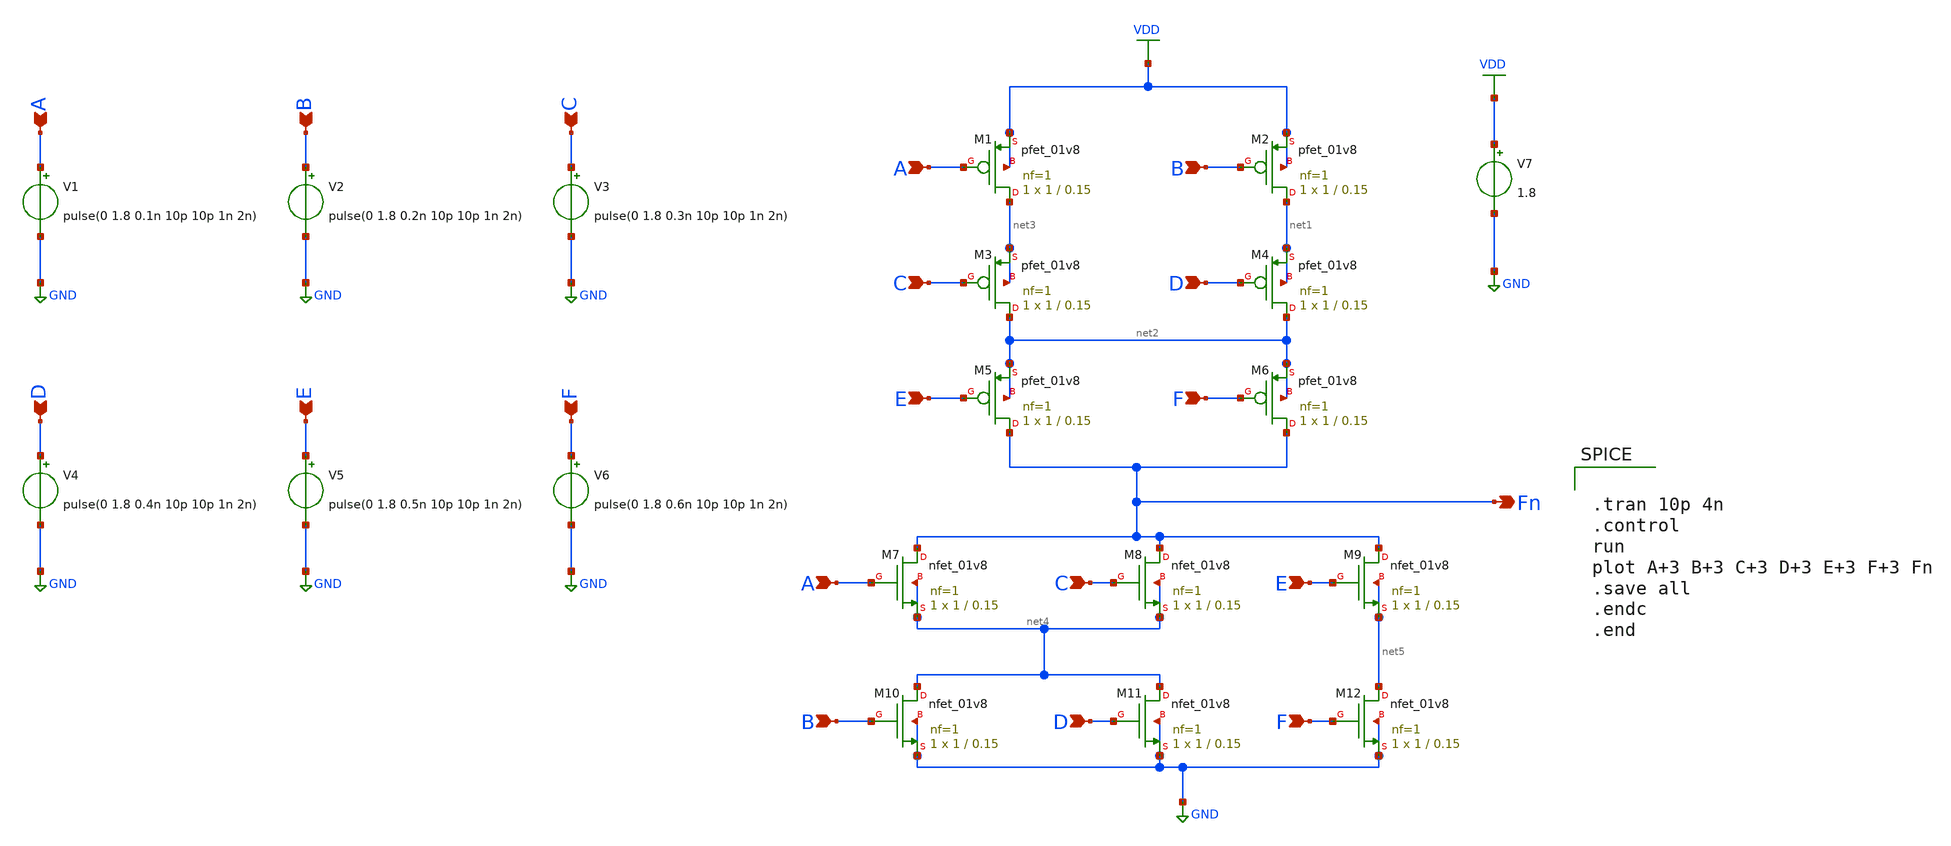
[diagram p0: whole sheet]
** sch_path: Week_1/Function_PreLayout/function_pre.sch
**.subckt function_pre A B A B C D E F A B C D E F Fn C D E F
*.ipin A
*.ipin B
*.ipin A
*.ipin B
*.ipin C
*.ipin D
*.ipin E
*.ipin F
*.ipin A
*.ipin B
*.ipin C
*.ipin D
*.ipin E
*.ipin F
*.opin Fn
*.ipin C
*.ipin D
*.ipin E
*.ipin F
V1 A GND pulse(0 1.8 0.1n 10p 10p 1n 2n)
V2 B GND pulse(0 1.8 0.2n 10p 10p 1n 2n)
XM1 net3 A VDD VDD sky130_fd_pr__pfet_01v8 L=0.15 W=1 nf=1 ad='int((nf+1)/2) * W/nf * 0.29' as='int((nf+2)/2) * W/nf * 0.29'
+ pd='2*int((nf+1)/2) * (W/nf + 0.29)' ps='2*int((nf+2)/2) * (W/nf + 0.29)' nrd='0.29 / W' nrs='0.29 / W'
+ sa=0 sb=0 sd=0 mult=1 m=1
XM2 net1 B VDD VDD sky130_fd_pr__pfet_01v8 L=0.15 W=1 nf=1 ad='int((nf+1)/2) * W/nf * 0.29' as='int((nf+2)/2) * W/nf * 0.29'
+ pd='2*int((nf+1)/2) * (W/nf + 0.29)' ps='2*int((nf+2)/2) * (W/nf + 0.29)' nrd='0.29 / W' nrs='0.29 / W'
+ sa=0 sb=0 sd=0 mult=1 m=1
XM3 net2 C net3 net3 sky130_fd_pr__pfet_01v8 L=0.15 W=1 nf=1 ad='int((nf+1)/2) * W/nf * 0.29' as='int((nf+2)/2) * W/nf * 0.29'
+ pd='2*int((nf+1)/2) * (W/nf + 0.29)' ps='2*int((nf+2)/2) * (W/nf + 0.29)' nrd='0.29 / W' nrs='0.29 / W'
+ sa=0 sb=0 sd=0 mult=1 m=1
XM4 net2 D net1 net1 sky130_fd_pr__pfet_01v8 L=0.15 W=1 nf=1 ad='int((nf+1)/2) * W/nf * 0.29' as='int((nf+2)/2) * W/nf * 0.29'
+ pd='2*int((nf+1)/2) * (W/nf + 0.29)' ps='2*int((nf+2)/2) * (W/nf + 0.29)' nrd='0.29 / W' nrs='0.29 / W'
+ sa=0 sb=0 sd=0 mult=1 m=1
XM5 Fn E net2 net2 sky130_fd_pr__pfet_01v8 L=0.15 W=1 nf=1 ad='int((nf+1)/2) * W/nf * 0.29' as='int((nf+2)/2) * W/nf * 0.29'
+ pd='2*int((nf+1)/2) * (W/nf + 0.29)' ps='2*int((nf+2)/2) * (W/nf + 0.29)' nrd='0.29 / W' nrs='0.29 / W'
+ sa=0 sb=0 sd=0 mult=1 m=1
XM6 Fn F net2 net2 sky130_fd_pr__pfet_01v8 L=0.15 W=1 nf=1 ad='int((nf+1)/2) * W/nf * 0.29' as='int((nf+2)/2) * W/nf * 0.29'
+ pd='2*int((nf+1)/2) * (W/nf + 0.29)' ps='2*int((nf+2)/2) * (W/nf + 0.29)' nrd='0.29 / W' nrs='0.29 / W'
+ sa=0 sb=0 sd=0 mult=1 m=1
XM7 Fn A net4 net4 sky130_fd_pr__nfet_01v8 L=0.15 W=1 nf=1 ad='int((nf+1)/2) * W/nf * 0.29' as='int((nf+2)/2) * W/nf * 0.29'
+ pd='2*int((nf+1)/2) * (W/nf + 0.29)' ps='2*int((nf+2)/2) * (W/nf + 0.29)' nrd='0.29 / W' nrs='0.29 / W'
+ sa=0 sb=0 sd=0 mult=1 m=1
XM8 Fn C net4 net4 sky130_fd_pr__nfet_01v8 L=0.15 W=1 nf=1 ad='int((nf+1)/2) * W/nf * 0.29' as='int((nf+2)/2) * W/nf * 0.29'
+ pd='2*int((nf+1)/2) * (W/nf + 0.29)' ps='2*int((nf+2)/2) * (W/nf + 0.29)' nrd='0.29 / W' nrs='0.29 / W'
+ sa=0 sb=0 sd=0 mult=1 m=1
XM9 Fn E net5 net5 sky130_fd_pr__nfet_01v8 L=0.15 W=1 nf=1 ad='int((nf+1)/2) * W/nf * 0.29' as='int((nf+2)/2) * W/nf * 0.29'
+ pd='2*int((nf+1)/2) * (W/nf + 0.29)' ps='2*int((nf+2)/2) * (W/nf + 0.29)' nrd='0.29 / W' nrs='0.29 / W'
+ sa=0 sb=0 sd=0 mult=1 m=1
XM10 net4 B GND GND sky130_fd_pr__nfet_01v8 L=0.15 W=1 nf=1 ad='int((nf+1)/2) * W/nf * 0.29' as='int((nf+2)/2) * W/nf * 0.29'
+ pd='2*int((nf+1)/2) * (W/nf + 0.29)' ps='2*int((nf+2)/2) * (W/nf + 0.29)' nrd='0.29 / W' nrs='0.29 / W'
+ sa=0 sb=0 sd=0 mult=1 m=1
XM11 net4 D GND GND sky130_fd_pr__nfet_01v8 L=0.15 W=1 nf=1 ad='int((nf+1)/2) * W/nf * 0.29' as='int((nf+2)/2) * W/nf * 0.29'
+ pd='2*int((nf+1)/2) * (W/nf + 0.29)' ps='2*int((nf+2)/2) * (W/nf + 0.29)' nrd='0.29 / W' nrs='0.29 / W'
+ sa=0 sb=0 sd=0 mult=1 m=1
XM12 net5 F GND GND sky130_fd_pr__nfet_01v8 L=0.15 W=1 nf=1 ad='int((nf+1)/2) * W/nf * 0.29' as='int((nf+2)/2) * W/nf * 0.29'
+ pd='2*int((nf+1)/2) * (W/nf + 0.29)' ps='2*int((nf+2)/2) * (W/nf + 0.29)' nrd='0.29 / W' nrs='0.29 / W'
+ sa=0 sb=0 sd=0 mult=1 m=1
V7 VDD GND 1.8
V3 C GND pulse(0 1.8 0.3n 10p 10p 1n 2n)
V4 D GND pulse(0 1.8 0.4n 10p 10p 1n 2n)
V5 E GND pulse(0 1.8 0.5n 10p 10p 1n 2n)
V6 F GND pulse(0 1.8 0.6n 10p 10p 1n 2n)
**** begin user architecture code


.lib /home/swagatika/open_pdks/sky130/sky130A/libs.tech/ngspice/sky130.lib.spice tt

.save all





.tran 10p 4n
.control
run
plot A+3 B+3 C+3 D+3 E+3 F+3 Fn
.save all
.endc
.end


**** end user architecture code
**.ends
.GLOBAL GND
.GLOBAL VDD
.end
